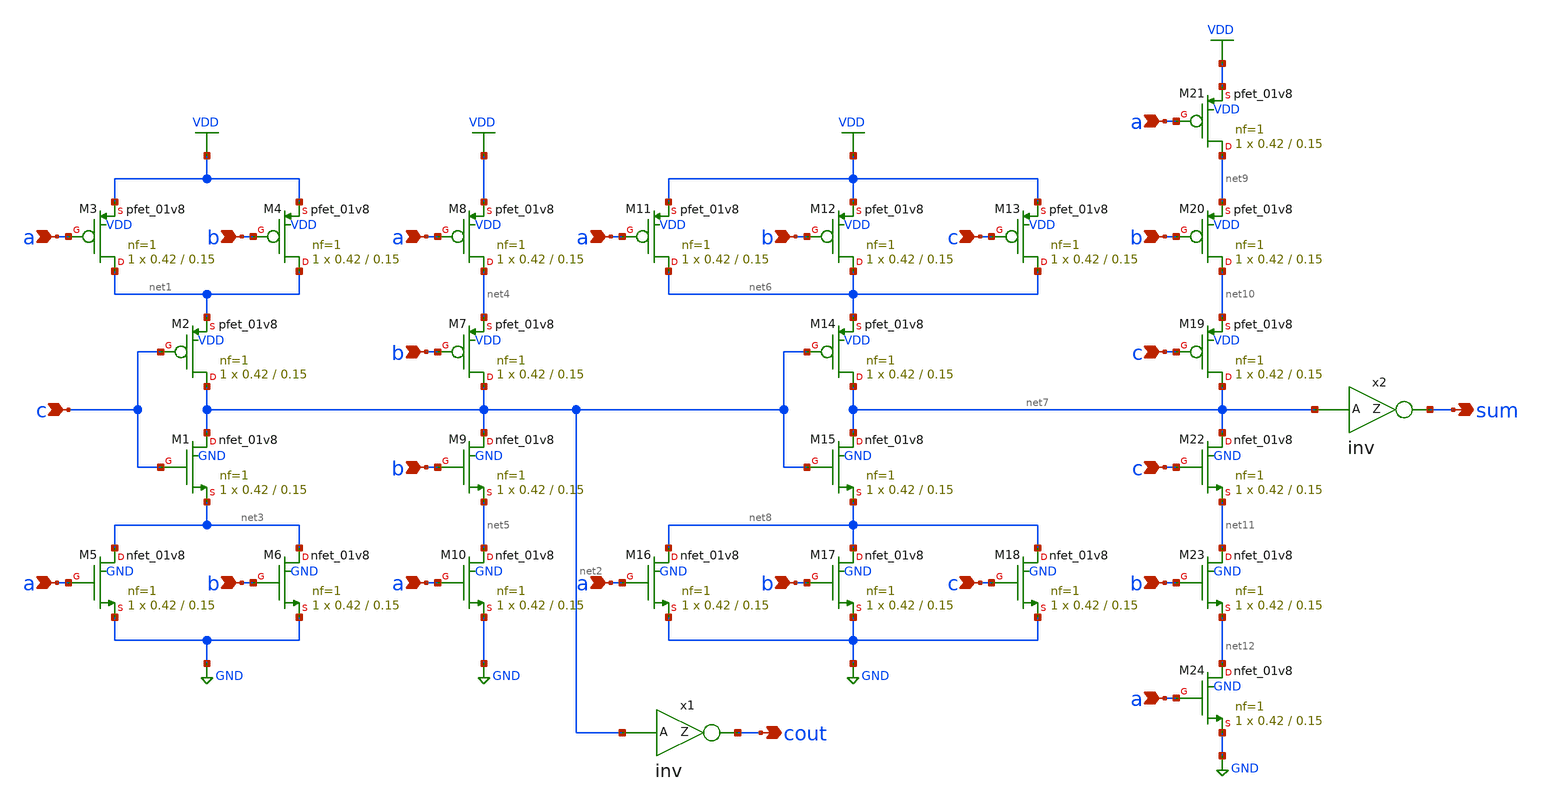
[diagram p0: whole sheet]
** sch_path: xschem/addf.sch
**.subckt addf a a a a a a a a b b b b b b b b c c c c c sum cout
*.ipin a
*.ipin a
*.ipin a
*.ipin a
*.ipin a
*.ipin a
*.ipin a
*.ipin a
*.ipin b
*.ipin b
*.ipin b
*.ipin b
*.ipin b
*.ipin b
*.ipin b
*.ipin b
*.ipin c
*.ipin c
*.ipin c
*.ipin c
*.ipin c
*.opin sum
*.opin cout
XM1 net2 c net3 GND sky130_fd_pr__nfet_01v8 L=0.15 W=0.42 nf=1 ad='int((nf+1)/2) * W/nf * 0.29' as='int((nf+2)/2) * W/nf * 0.29'
+ pd='2*int((nf+1)/2) * (W/nf + 0.29)' ps='2*int((nf+2)/2) * (W/nf + 0.29)' nrd='0.29 / W' nrs='0.29 / W'
+ sa=0 sb=0 sd=0 mult=1 m=1
XM2 net2 c net1 VDD sky130_fd_pr__pfet_01v8 L=0.15 W=0.42 nf=1 ad='int((nf+1)/2) * W/nf * 0.29' as='int((nf+2)/2) * W/nf * 0.29'
+ pd='2*int((nf+1)/2) * (W/nf + 0.29)' ps='2*int((nf+2)/2) * (W/nf + 0.29)' nrd='0.29 / W' nrs='0.29 / W'
+ sa=0 sb=0 sd=0 mult=1 m=1
XM3 net1 a VDD VDD sky130_fd_pr__pfet_01v8 L=0.15 W=0.42 nf=1 ad='int((nf+1)/2) * W/nf * 0.29' as='int((nf+2)/2) * W/nf * 0.29'
+ pd='2*int((nf+1)/2) * (W/nf + 0.29)' ps='2*int((nf+2)/2) * (W/nf + 0.29)' nrd='0.29 / W' nrs='0.29 / W'
+ sa=0 sb=0 sd=0 mult=1 m=1
XM4 net1 b VDD VDD sky130_fd_pr__pfet_01v8 L=0.15 W=0.42 nf=1 ad='int((nf+1)/2) * W/nf * 0.29' as='int((nf+2)/2) * W/nf * 0.29'
+ pd='2*int((nf+1)/2) * (W/nf + 0.29)' ps='2*int((nf+2)/2) * (W/nf + 0.29)' nrd='0.29 / W' nrs='0.29 / W'
+ sa=0 sb=0 sd=0 mult=1 m=1
XM5 net3 a GND GND sky130_fd_pr__nfet_01v8 L=0.15 W=0.42 nf=1 ad='int((nf+1)/2) * W/nf * 0.29' as='int((nf+2)/2) * W/nf * 0.29'
+ pd='2*int((nf+1)/2) * (W/nf + 0.29)' ps='2*int((nf+2)/2) * (W/nf + 0.29)' nrd='0.29 / W' nrs='0.29 / W'
+ sa=0 sb=0 sd=0 mult=1 m=1
XM6 net3 b GND GND sky130_fd_pr__nfet_01v8 L=0.15 W=0.42 nf=1 ad='int((nf+1)/2) * W/nf * 0.29' as='int((nf+2)/2) * W/nf * 0.29'
+ pd='2*int((nf+1)/2) * (W/nf + 0.29)' ps='2*int((nf+2)/2) * (W/nf + 0.29)' nrd='0.29 / W' nrs='0.29 / W'
+ sa=0 sb=0 sd=0 mult=1 m=1
XM7 net2 b net4 VDD sky130_fd_pr__pfet_01v8 L=0.15 W=0.42 nf=1 ad='int((nf+1)/2) * W/nf * 0.29' as='int((nf+2)/2) * W/nf * 0.29'
+ pd='2*int((nf+1)/2) * (W/nf + 0.29)' ps='2*int((nf+2)/2) * (W/nf + 0.29)' nrd='0.29 / W' nrs='0.29 / W'
+ sa=0 sb=0 sd=0 mult=1 m=1
XM8 net4 a VDD VDD sky130_fd_pr__pfet_01v8 L=0.15 W=0.42 nf=1 ad='int((nf+1)/2) * W/nf * 0.29' as='int((nf+2)/2) * W/nf * 0.29'
+ pd='2*int((nf+1)/2) * (W/nf + 0.29)' ps='2*int((nf+2)/2) * (W/nf + 0.29)' nrd='0.29 / W' nrs='0.29 / W'
+ sa=0 sb=0 sd=0 mult=1 m=1
XM9 net2 b net5 GND sky130_fd_pr__nfet_01v8 L=0.15 W=0.42 nf=1 ad='int((nf+1)/2) * W/nf * 0.29' as='int((nf+2)/2) * W/nf * 0.29'
+ pd='2*int((nf+1)/2) * (W/nf + 0.29)' ps='2*int((nf+2)/2) * (W/nf + 0.29)' nrd='0.29 / W' nrs='0.29 / W'
+ sa=0 sb=0 sd=0 mult=1 m=1
XM10 net5 a GND GND sky130_fd_pr__nfet_01v8 L=0.15 W=0.42 nf=1 ad='int((nf+1)/2) * W/nf * 0.29' as='int((nf+2)/2) * W/nf * 0.29'
+ pd='2*int((nf+1)/2) * (W/nf + 0.29)' ps='2*int((nf+2)/2) * (W/nf + 0.29)' nrd='0.29 / W' nrs='0.29 / W'
+ sa=0 sb=0 sd=0 mult=1 m=1
XM11 net6 a VDD VDD sky130_fd_pr__pfet_01v8 L=0.15 W=0.42 nf=1 ad='int((nf+1)/2) * W/nf * 0.29' as='int((nf+2)/2) * W/nf * 0.29'
+ pd='2*int((nf+1)/2) * (W/nf + 0.29)' ps='2*int((nf+2)/2) * (W/nf + 0.29)' nrd='0.29 / W' nrs='0.29 / W'
+ sa=0 sb=0 sd=0 mult=1 m=1
XM12 net6 b VDD VDD sky130_fd_pr__pfet_01v8 L=0.15 W=0.42 nf=1 ad='int((nf+1)/2) * W/nf * 0.29' as='int((nf+2)/2) * W/nf * 0.29'
+ pd='2*int((nf+1)/2) * (W/nf + 0.29)' ps='2*int((nf+2)/2) * (W/nf + 0.29)' nrd='0.29 / W' nrs='0.29 / W'
+ sa=0 sb=0 sd=0 mult=1 m=1
XM13 net6 c VDD VDD sky130_fd_pr__pfet_01v8 L=0.15 W=0.42 nf=1 ad='int((nf+1)/2) * W/nf * 0.29' as='int((nf+2)/2) * W/nf * 0.29'
+ pd='2*int((nf+1)/2) * (W/nf + 0.29)' ps='2*int((nf+2)/2) * (W/nf + 0.29)' nrd='0.29 / W' nrs='0.29 / W'
+ sa=0 sb=0 sd=0 mult=1 m=1
XM14 net7 net2 net6 VDD sky130_fd_pr__pfet_01v8 L=0.15 W=0.42 nf=1 ad='int((nf+1)/2) * W/nf * 0.29' as='int((nf+2)/2) * W/nf * 0.29'
+ pd='2*int((nf+1)/2) * (W/nf + 0.29)' ps='2*int((nf+2)/2) * (W/nf + 0.29)' nrd='0.29 / W' nrs='0.29 / W'
+ sa=0 sb=0 sd=0 mult=1 m=1
XM15 net7 net2 net8 GND sky130_fd_pr__nfet_01v8 L=0.15 W=0.42 nf=1 ad='int((nf+1)/2) * W/nf * 0.29' as='int((nf+2)/2) * W/nf * 0.29'
+ pd='2*int((nf+1)/2) * (W/nf + 0.29)' ps='2*int((nf+2)/2) * (W/nf + 0.29)' nrd='0.29 / W' nrs='0.29 / W'
+ sa=0 sb=0 sd=0 mult=1 m=1
XM16 net8 a GND GND sky130_fd_pr__nfet_01v8 L=0.15 W=0.42 nf=1 ad='int((nf+1)/2) * W/nf * 0.29' as='int((nf+2)/2) * W/nf * 0.29'
+ pd='2*int((nf+1)/2) * (W/nf + 0.29)' ps='2*int((nf+2)/2) * (W/nf + 0.29)' nrd='0.29 / W' nrs='0.29 / W'
+ sa=0 sb=0 sd=0 mult=1 m=1
XM17 net8 b GND GND sky130_fd_pr__nfet_01v8 L=0.15 W=0.42 nf=1 ad='int((nf+1)/2) * W/nf * 0.29' as='int((nf+2)/2) * W/nf * 0.29'
+ pd='2*int((nf+1)/2) * (W/nf + 0.29)' ps='2*int((nf+2)/2) * (W/nf + 0.29)' nrd='0.29 / W' nrs='0.29 / W'
+ sa=0 sb=0 sd=0 mult=1 m=1
XM18 net8 c GND GND sky130_fd_pr__nfet_01v8 L=0.15 W=0.42 nf=1 ad='int((nf+1)/2) * W/nf * 0.29' as='int((nf+2)/2) * W/nf * 0.29'
+ pd='2*int((nf+1)/2) * (W/nf + 0.29)' ps='2*int((nf+2)/2) * (W/nf + 0.29)' nrd='0.29 / W' nrs='0.29 / W'
+ sa=0 sb=0 sd=0 mult=1 m=1
XM19 net7 c net10 VDD sky130_fd_pr__pfet_01v8 L=0.15 W=0.42 nf=1 ad='int((nf+1)/2) * W/nf * 0.29' as='int((nf+2)/2) * W/nf * 0.29'
+ pd='2*int((nf+1)/2) * (W/nf + 0.29)' ps='2*int((nf+2)/2) * (W/nf + 0.29)' nrd='0.29 / W' nrs='0.29 / W'
+ sa=0 sb=0 sd=0 mult=1 m=1
XM20 net10 b net9 VDD sky130_fd_pr__pfet_01v8 L=0.15 W=0.42 nf=1 ad='int((nf+1)/2) * W/nf * 0.29' as='int((nf+2)/2) * W/nf * 0.29'
+ pd='2*int((nf+1)/2) * (W/nf + 0.29)' ps='2*int((nf+2)/2) * (W/nf + 0.29)' nrd='0.29 / W' nrs='0.29 / W'
+ sa=0 sb=0 sd=0 mult=1 m=1
XM21 net9 a VDD VDD sky130_fd_pr__pfet_01v8 L=0.15 W=0.42 nf=1 ad='int((nf+1)/2) * W/nf * 0.29' as='int((nf+2)/2) * W/nf * 0.29'
+ pd='2*int((nf+1)/2) * (W/nf + 0.29)' ps='2*int((nf+2)/2) * (W/nf + 0.29)' nrd='0.29 / W' nrs='0.29 / W'
+ sa=0 sb=0 sd=0 mult=1 m=1
XM22 net7 c net11 GND sky130_fd_pr__nfet_01v8 L=0.15 W=0.42 nf=1 ad='int((nf+1)/2) * W/nf * 0.29' as='int((nf+2)/2) * W/nf * 0.29'
+ pd='2*int((nf+1)/2) * (W/nf + 0.29)' ps='2*int((nf+2)/2) * (W/nf + 0.29)' nrd='0.29 / W' nrs='0.29 / W'
+ sa=0 sb=0 sd=0 mult=1 m=1
XM23 net11 b net12 GND sky130_fd_pr__nfet_01v8 L=0.15 W=0.42 nf=1 ad='int((nf+1)/2) * W/nf * 0.29' as='int((nf+2)/2) * W/nf * 0.29'
+ pd='2*int((nf+1)/2) * (W/nf + 0.29)' ps='2*int((nf+2)/2) * (W/nf + 0.29)' nrd='0.29 / W' nrs='0.29 / W'
+ sa=0 sb=0 sd=0 mult=1 m=1
XM24 net12 a GND GND sky130_fd_pr__nfet_01v8 L=0.15 W=0.42 nf=1 ad='int((nf+1)/2) * W/nf * 0.29' as='int((nf+2)/2) * W/nf * 0.29'
+ pd='2*int((nf+1)/2) * (W/nf + 0.29)' ps='2*int((nf+2)/2) * (W/nf + 0.29)' nrd='0.29 / W' nrs='0.29 / W'
+ sa=0 sb=0 sd=0 mult=1 m=1
x1 cout net2 inv
x2 sum net7 inv
**.ends

* expanding   symbol:  inv.sym # of pins=2
** sym_path: xschem/inv.sym
** sch_path: xschem/inv.sch
.subckt inv Z A
*.ipin a
*.opin z
XM1 z a GND GND sky130_fd_pr__nfet_01v8 L=0.15 W=0.42 nf=1 ad='int((nf+1)/2) * W/nf * 0.29' as='int((nf+2)/2) * W/nf * 0.29'
+ pd='2*int((nf+1)/2) * (W/nf + 0.29)' ps='2*int((nf+2)/2) * (W/nf + 0.29)' nrd='0.29 / W' nrs='0.29 / W'
+ sa=0 sb=0 sd=0 mult=1 m=1
XM2 z a VDD VDD sky130_fd_pr__pfet_01v8 L=0.15 W=0.84 nf=1 ad='int((nf+1)/2) * W/nf * 0.29' as='int((nf+2)/2) * W/nf * 0.29'
+ pd='2*int((nf+1)/2) * (W/nf + 0.29)' ps='2*int((nf+2)/2) * (W/nf + 0.29)' nrd='0.29 / W' nrs='0.29 / W'
+ sa=0 sb=0 sd=0 mult=1 m=1
.ends

.GLOBAL VDD
.GLOBAL GND
.end
